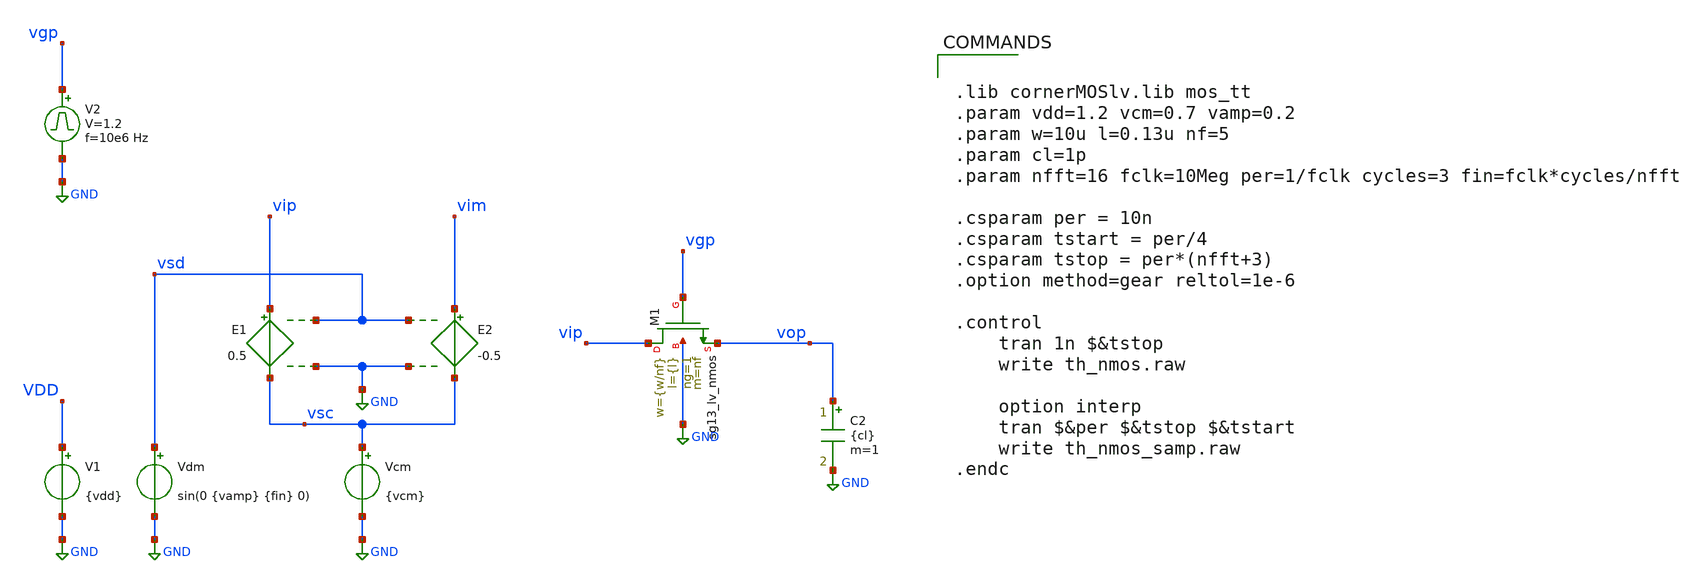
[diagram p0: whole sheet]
** sch_path: th_nmos/xschem/th_nmos.sch
**.subckt th_nmos
E1 vip vsc vsd GND 0.5
E2 vim vsc vsd GND -0.5
Vcm vsc GND {vcm}
V1 VDD GND {vdd}
XM1 vip vgp vop GND sg13_lv_nmos w={w/nf} l={l} ng=1 m=nf mm_ok=1
C2 vop GND {cl} m=1
V2 vgp GND pulse 0 1.2 '0.495/ 10e6 ' '0.01/10e6 ' '0.01/10e6 ' '0.49/10e6 ' '1/10e6 '
Vdm vsd GND sin(0 {vamp} {fin} 0)
**** begin user architecture code


.lib cornerMOSlv.lib mos_tt
.param vdd=1.2 vcm=0.7 vamp=0.2
.param w=10u l=0.13u nf=5
.param cl=1p
.param nfft=16 fclk=10Meg per=1/fclk cycles=3 fin=fclk*cycles/nfft

.csparam per = 10n
.csparam tstart = per/4
.csparam tstop = per*(nfft+3)
.option method=gear reltol=1e-6

.control
    tran 1n $&tstop
    write th_nmos.raw

    option interp
    tran $&per $&tstop $&tstart
    write th_nmos_samp.raw
.endc


**** end user architecture code
**.ends
.GLOBAL GND
.end
